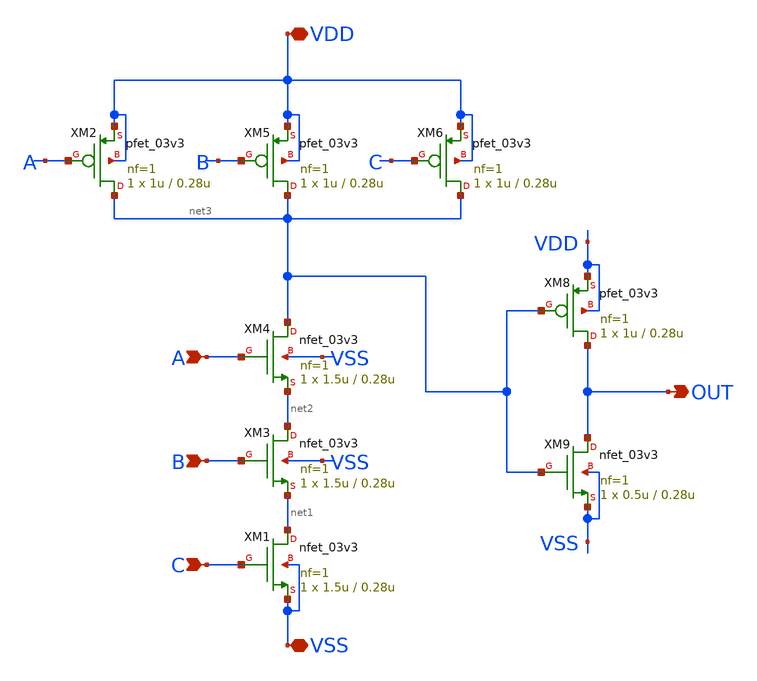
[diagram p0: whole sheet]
** sch_path: SCOP_INPUT_AND_MUX_PAKISTAN_03/Xschem/Logic_Gates/AND_3_Input.sch
**.subckt AND_3_Input VDD VSS A B C OUT
*.iopin VDD
*.iopin VSS
*.ipin A
*.ipin B
*.ipin C
*.opin OUT
XM1 net1 C VSS VSS nfet_03v3 L=0.28u W=1.5u nf=1 ad='int((nf+1)/2) * W/nf * 0.18u' as='int((nf+2)/2) * W/nf * 0.18u'
+ pd='2*int((nf+1)/2) * (W/nf + 0.18u)' ps='2*int((nf+2)/2) * (W/nf + 0.18u)' nrd='0.18u / W' nrs='0.18u / W'
+ sa=0 sb=0 sd=0 m=1
XM2 net3 A VDD VDD pfet_03v3 L=0.28u W=1u nf=1 ad='int((nf+1)/2) * W/nf * 0.18u' as='int((nf+2)/2) * W/nf * 0.18u'
+ pd='2*int((nf+1)/2) * (W/nf + 0.18u)' ps='2*int((nf+2)/2) * (W/nf + 0.18u)' nrd='0.18u / W' nrs='0.18u / W'
+ sa=0 sb=0 sd=0 m=1
XM3 net2 B net1 VSS nfet_03v3 L=0.28u W=1.5u nf=1 ad='int((nf+1)/2) * W/nf * 0.18u' as='int((nf+2)/2) * W/nf * 0.18u'
+ pd='2*int((nf+1)/2) * (W/nf + 0.18u)' ps='2*int((nf+2)/2) * (W/nf + 0.18u)' nrd='0.18u / W' nrs='0.18u / W'
+ sa=0 sb=0 sd=0 m=1
XM4 net3 A net2 VSS nfet_03v3 L=0.28u W=1.5u nf=1 ad='int((nf+1)/2) * W/nf * 0.18u' as='int((nf+2)/2) * W/nf * 0.18u'
+ pd='2*int((nf+1)/2) * (W/nf + 0.18u)' ps='2*int((nf+2)/2) * (W/nf + 0.18u)' nrd='0.18u / W' nrs='0.18u / W'
+ sa=0 sb=0 sd=0 m=1
XM5 net3 B VDD VDD pfet_03v3 L=0.28u W=1u nf=1 ad='int((nf+1)/2) * W/nf * 0.18u' as='int((nf+2)/2) * W/nf * 0.18u'
+ pd='2*int((nf+1)/2) * (W/nf + 0.18u)' ps='2*int((nf+2)/2) * (W/nf + 0.18u)' nrd='0.18u / W' nrs='0.18u / W'
+ sa=0 sb=0 sd=0 m=1
XM6 net3 C VDD VDD pfet_03v3 L=0.28u W=1u nf=1 ad='int((nf+1)/2) * W/nf * 0.18u' as='int((nf+2)/2) * W/nf * 0.18u'
+ pd='2*int((nf+1)/2) * (W/nf + 0.18u)' ps='2*int((nf+2)/2) * (W/nf + 0.18u)' nrd='0.18u / W' nrs='0.18u / W'
+ sa=0 sb=0 sd=0 m=1
XM8 OUT net3 VDD VDD pfet_03v3 L=0.28u W=1u nf=1 ad='int((nf+1)/2) * W/nf * 0.18u' as='int((nf+2)/2) * W/nf * 0.18u'
+ pd='2*int((nf+1)/2) * (W/nf + 0.18u)' ps='2*int((nf+2)/2) * (W/nf + 0.18u)' nrd='0.18u / W' nrs='0.18u / W'
+ sa=0 sb=0 sd=0 m=1
XM9 OUT net3 VSS VSS nfet_03v3 L=0.28u W=0.5u nf=1 ad='int((nf+1)/2) * W/nf * 0.18u' as='int((nf+2)/2) * W/nf * 0.18u'
+ pd='2*int((nf+1)/2) * (W/nf + 0.18u)' ps='2*int((nf+2)/2) * (W/nf + 0.18u)' nrd='0.18u / W' nrs='0.18u / W'
+ sa=0 sb=0 sd=0 m=1
**.ends
.end
